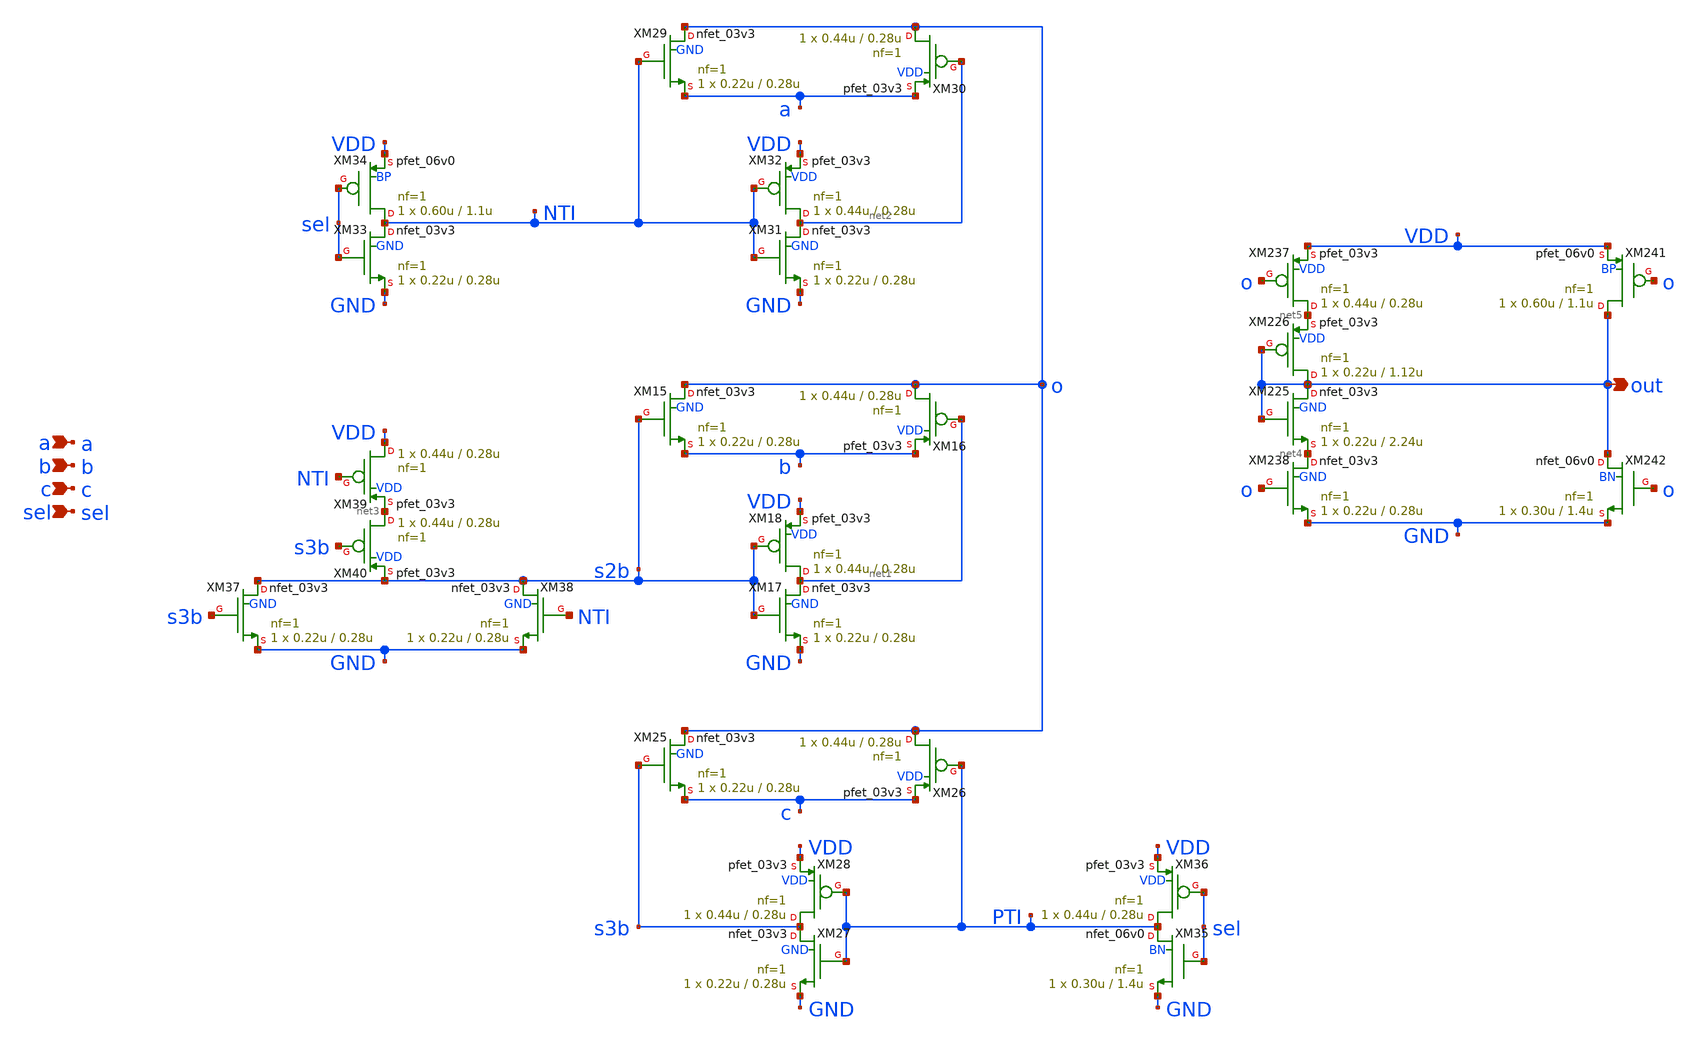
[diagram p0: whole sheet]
** sch_path: xschem_designs/MUX3.sch
**.subckt MUX3 a b c sel out
*.ipin a
*.ipin b
*.ipin c
*.ipin sel
*.opin out
XM15 o s2b b GND nfet_03v3 L=0.28u W=0.22u nf=1 ad='int((nf+1)/2) * W/nf * 0.18u' as='int((nf+2)/2) * W/nf * 0.18u'
+ pd='2*int((nf+1)/2) * (W/nf + 0.18u)' ps='2*int((nf+2)/2) * (W/nf + 0.18u)' nrd='0.18u / W' nrs='0.18u / W'
+ sa=0 sb=0 sd=0 m=1 par=1
XM16 o net1 b VDD pfet_03v3 L=0.28u W=0.44u nf=1 ad='int((nf+1)/2) * W/nf * 0.18u' as='int((nf+2)/2) * W/nf * 0.18u'
+ pd='2*int((nf+1)/2) * (W/nf + 0.18u)' ps='2*int((nf+2)/2) * (W/nf + 0.18u)' nrd='0.18u / W' nrs='0.18u / W'
+ sa=0 sb=0 sd=0 m=1 par=1
XM17 net1 s2b GND GND nfet_03v3 L=0.28u W=0.22u nf=1 ad='int((nf+1)/2) * W/nf * 0.18u' as='int((nf+2)/2) * W/nf * 0.18u'
+ pd='2*int((nf+1)/2) * (W/nf + 0.18u)' ps='2*int((nf+2)/2) * (W/nf + 0.18u)' nrd='0.18u / W' nrs='0.18u / W'
+ sa=0 sb=0 sd=0 m=1 par=1
XM18 net1 s2b VDD VDD pfet_03v3 L=0.28u W=0.44u nf=1 ad='int((nf+1)/2) * W/nf * 0.18u' as='int((nf+2)/2) * W/nf * 0.18u'
+ pd='2*int((nf+1)/2) * (W/nf + 0.18u)' ps='2*int((nf+2)/2) * (W/nf + 0.18u)' nrd='0.18u / W' nrs='0.18u / W'
+ sa=0 sb=0 sd=0 m=1 par=1
XM25 o s3b c GND nfet_03v3 L=0.28u W=0.22u nf=1 ad='int((nf+1)/2) * W/nf * 0.18u' as='int((nf+2)/2) * W/nf * 0.18u'
+ pd='2*int((nf+1)/2) * (W/nf + 0.18u)' ps='2*int((nf+2)/2) * (W/nf + 0.18u)' nrd='0.18u / W' nrs='0.18u / W'
+ sa=0 sb=0 sd=0 m=1 par=1
XM26 o PTI c VDD pfet_03v3 L=0.28u W=0.44u nf=1 ad='int((nf+1)/2) * W/nf * 0.18u' as='int((nf+2)/2) * W/nf * 0.18u'
+ pd='2*int((nf+1)/2) * (W/nf + 0.18u)' ps='2*int((nf+2)/2) * (W/nf + 0.18u)' nrd='0.18u / W' nrs='0.18u / W'
+ sa=0 sb=0 sd=0 m=1 par=1
XM27 s3b PTI GND GND nfet_03v3 L=0.28u W=0.22u nf=1 ad='int((nf+1)/2) * W/nf * 0.18u' as='int((nf+2)/2) * W/nf * 0.18u'
+ pd='2*int((nf+1)/2) * (W/nf + 0.18u)' ps='2*int((nf+2)/2) * (W/nf + 0.18u)' nrd='0.18u / W' nrs='0.18u / W'
+ sa=0 sb=0 sd=0 m=1 par=1
XM28 s3b PTI VDD VDD pfet_03v3 L=0.28u W=0.44u nf=1 ad='int((nf+1)/2) * W/nf * 0.18u' as='int((nf+2)/2) * W/nf * 0.18u'
+ pd='2*int((nf+1)/2) * (W/nf + 0.18u)' ps='2*int((nf+2)/2) * (W/nf + 0.18u)' nrd='0.18u / W' nrs='0.18u / W'
+ sa=0 sb=0 sd=0 m=1 par=1
XM29 o NTI a GND nfet_03v3 L=0.28u W=0.22u nf=1 ad='int((nf+1)/2) * W/nf * 0.18u' as='int((nf+2)/2) * W/nf * 0.18u'
+ pd='2*int((nf+1)/2) * (W/nf + 0.18u)' ps='2*int((nf+2)/2) * (W/nf + 0.18u)' nrd='0.18u / W' nrs='0.18u / W'
+ sa=0 sb=0 sd=0 m=1 par=1
XM30 o net2 a VDD pfet_03v3 L=0.28u W=0.44u nf=1 ad='int((nf+1)/2) * W/nf * 0.18u' as='int((nf+2)/2) * W/nf * 0.18u'
+ pd='2*int((nf+1)/2) * (W/nf + 0.18u)' ps='2*int((nf+2)/2) * (W/nf + 0.18u)' nrd='0.18u / W' nrs='0.18u / W'
+ sa=0 sb=0 sd=0 m=1 par=1
XM31 net2 NTI GND GND nfet_03v3 L=0.28u W=0.22u nf=1 ad='int((nf+1)/2) * W/nf * 0.18u' as='int((nf+2)/2) * W/nf * 0.18u'
+ pd='2*int((nf+1)/2) * (W/nf + 0.18u)' ps='2*int((nf+2)/2) * (W/nf + 0.18u)' nrd='0.18u / W' nrs='0.18u / W'
+ sa=0 sb=0 sd=0 m=1 par=1
XM32 net2 NTI VDD VDD pfet_03v3 L=0.28u W=0.44u nf=1 ad='int((nf+1)/2) * W/nf * 0.18u' as='int((nf+2)/2) * W/nf * 0.18u'
+ pd='2*int((nf+1)/2) * (W/nf + 0.18u)' ps='2*int((nf+2)/2) * (W/nf + 0.18u)' nrd='0.18u / W' nrs='0.18u / W'
+ sa=0 sb=0 sd=0 m=1 par=1
XM33 NTI sel GND GND nfet_03v3 L=0.28u W=0.22u nf=1 ad='int((nf+1)/2) * W/nf * 0.18u' as='int((nf+2)/2) * W/nf * 0.18u'
+ pd='2*int((nf+1)/2) * (W/nf + 0.18u)' ps='2*int((nf+2)/2) * (W/nf + 0.18u)' nrd='0.18u / W' nrs='0.18u / W'
+ sa=0 sb=0 sd=0 m=1 par=1
XM34 NTI sel VDD BP pfet_06v0 L=1.1u W=0.60u nf=1 ad='int((nf+1)/2) * W/nf * 0.18u' as='int((nf+2)/2) * W/nf * 0.18u'
+ pd='2*int((nf+1)/2) * (W/nf + 0.18u)' ps='2*int((nf+2)/2) * (W/nf + 0.18u)' nrd='0.18u / W' nrs='0.18u / W'
+ sa=0 sb=0 sd=0 m=1 par=1
XM35 PTI sel GND BN nfet_06v0 L=1.4u W=0.30u nf=1 ad='int((nf+1)/2) * W/nf * 0.18u' as='int((nf+2)/2) * W/nf * 0.18u'
+ pd='2*int((nf+1)/2) * (W/nf + 0.18u)' ps='2*int((nf+2)/2) * (W/nf + 0.18u)' nrd='0.18u / W' nrs='0.18u / W'
+ sa=0 sb=0 sd=0 m=1 par=1
XM36 PTI sel VDD VDD pfet_03v3 L=0.28u W=0.44u nf=1 ad='int((nf+1)/2) * W/nf * 0.18u' as='int((nf+2)/2) * W/nf * 0.18u'
+ pd='2*int((nf+1)/2) * (W/nf + 0.18u)' ps='2*int((nf+2)/2) * (W/nf + 0.18u)' nrd='0.18u / W' nrs='0.18u / W'
+ sa=0 sb=0 sd=0 m=1 par=1
XM37 s2b s3b GND GND nfet_03v3 L=0.28u W=0.22u nf=1 ad='int((nf+1)/2) * W/nf * 0.18u' as='int((nf+2)/2) * W/nf * 0.18u'
+ pd='2*int((nf+1)/2) * (W/nf + 0.18u)' ps='2*int((nf+2)/2) * (W/nf + 0.18u)' nrd='0.18u / W' nrs='0.18u / W'
+ sa=0 sb=0 sd=0 m=1 par=1
XM38 s2b NTI GND GND nfet_03v3 L=0.28u W=0.22u nf=1 ad='int((nf+1)/2) * W/nf * 0.18u' as='int((nf+2)/2) * W/nf * 0.18u'
+ pd='2*int((nf+1)/2) * (W/nf + 0.18u)' ps='2*int((nf+2)/2) * (W/nf + 0.18u)' nrd='0.18u / W' nrs='0.18u / W'
+ sa=0 sb=0 sd=0 m=1 par=1
XM39 VDD NTI net3 VDD pfet_03v3 L=0.28u W=0.44u nf=1 ad='int((nf+1)/2) * W/nf * 0.18u' as='int((nf+2)/2) * W/nf * 0.18u'
+ pd='2*int((nf+1)/2) * (W/nf + 0.18u)' ps='2*int((nf+2)/2) * (W/nf + 0.18u)' nrd='0.18u / W' nrs='0.18u / W'
+ sa=0 sb=0 sd=0 m=1 par=1
XM40 net3 s3b s2b VDD pfet_03v3 L=0.28u W=0.44u nf=1 ad='int((nf+1)/2) * W/nf * 0.18u' as='int((nf+2)/2) * W/nf * 0.18u'
+ pd='2*int((nf+1)/2) * (W/nf + 0.18u)' ps='2*int((nf+2)/2) * (W/nf + 0.18u)' nrd='0.18u / W' nrs='0.18u / W'
+ sa=0 sb=0 sd=0 m=1 par=1
XM225 out out net4 GND nfet_03v3 L=2.24u W=0.22u nf=1 ad='int((nf+1)/2) * W/nf * 0.18u' as='int((nf+2)/2) * W/nf * 0.18u'
+ pd='2*int((nf+1)/2) * (W/nf + 0.18u)' ps='2*int((nf+2)/2) * (W/nf + 0.18u)' nrd='0.18u / W' nrs='0.18u / W'
+ sa=0 sb=0 sd=0 m=1 par=1
XM226 out out net5 VDD pfet_03v3 L=1.12u W=0.22u nf=1 ad='int((nf+1)/2) * W/nf * 0.18u' as='int((nf+2)/2) * W/nf * 0.18u'
+ pd='2*int((nf+1)/2) * (W/nf + 0.18u)' ps='2*int((nf+2)/2) * (W/nf + 0.18u)' nrd='0.18u / W' nrs='0.18u / W'
+ sa=0 sb=0 sd=0 m=1 par=1
XM237 net5 o VDD VDD pfet_03v3 L=0.28u W=0.44u nf=1 ad='int((nf+1)/2) * W/nf * 0.18u' as='int((nf+2)/2) * W/nf * 0.18u'
+ pd='2*int((nf+1)/2) * (W/nf + 0.18u)' ps='2*int((nf+2)/2) * (W/nf + 0.18u)' nrd='0.18u / W' nrs='0.18u / W'
+ sa=0 sb=0 sd=0 m=1 par=1
XM238 net4 o GND GND nfet_03v3 L=0.28u W=0.22u nf=1 ad='int((nf+1)/2) * W/nf * 0.18u' as='int((nf+2)/2) * W/nf * 0.18u'
+ pd='2*int((nf+1)/2) * (W/nf + 0.18u)' ps='2*int((nf+2)/2) * (W/nf + 0.18u)' nrd='0.18u / W' nrs='0.18u / W'
+ sa=0 sb=0 sd=0 m=1 par=1
XM241 out o VDD BP pfet_06v0 L=1.1u W=0.60u nf=1 ad='int((nf+1)/2) * W/nf * 0.18u' as='int((nf+2)/2) * W/nf * 0.18u'
+ pd='2*int((nf+1)/2) * (W/nf + 0.18u)' ps='2*int((nf+2)/2) * (W/nf + 0.18u)' nrd='0.18u / W' nrs='0.18u / W'
+ sa=0 sb=0 sd=0 m=1 par=1
XM242 out o GND BN nfet_06v0 L=1.4u W=0.30u nf=1 ad='int((nf+1)/2) * W/nf * 0.18u' as='int((nf+2)/2) * W/nf * 0.18u'
+ pd='2*int((nf+1)/2) * (W/nf + 0.18u)' ps='2*int((nf+2)/2) * (W/nf + 0.18u)' nrd='0.18u / W' nrs='0.18u / W'
+ sa=0 sb=0 sd=0 m=1 par=1
**.ends
.end
